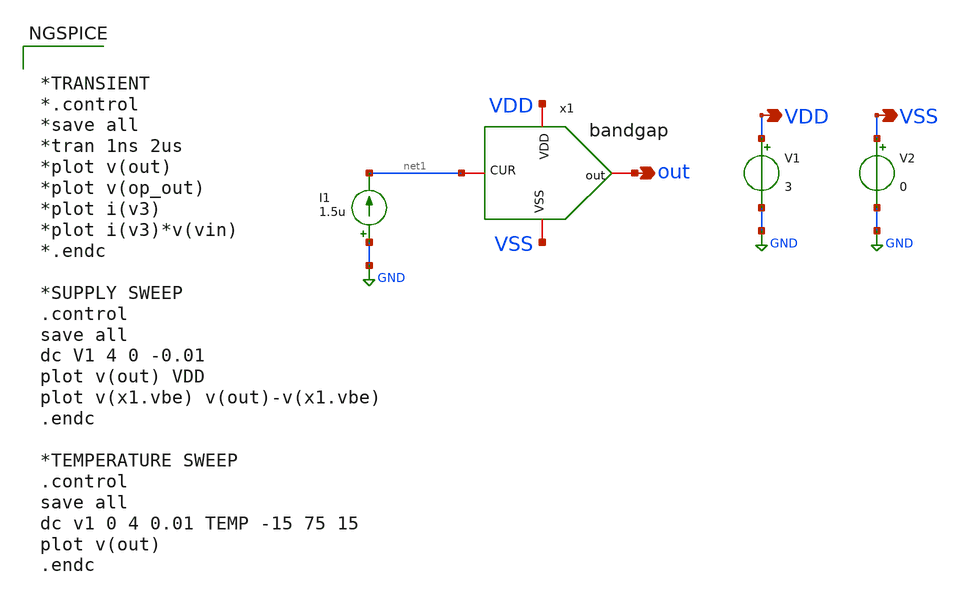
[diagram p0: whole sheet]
** sch_path: LDO/xschem/bandgap/bandgap-test.sch

.include $env(PDK_ROOT)/$env(PDK)/libs.tech/ngspice/design.ngspice
.lib $env(PDK_ROOT)/$env(PDK)/libs.tech/ngspice/sm141064.ngspice typical
.lib $env(PDK_ROOT)/$env(PDK)/libs.tech/ngspice/sm141064.ngspice mimcap_statistical
.lib $env(PDK_ROOT)/$env(PDK)/libs.tech/ngspice/sm141064.ngspice cap_mim
.lib $env(PDK_ROOT)/$env(PDK)/libs.tech/ngspice/sm141064.ngspice res_typical
.lib $env(PDK_ROOT)/$env(PDK)/libs.tech/ngspice/sm141064.ngspice bjt_typical
.lib $env(PDK_ROOT)/$env(PDK)/libs.tech/ngspice/sm141064.ngspice moscap_typical

**.subckt bandgap-test VDD VSS out
*.opin VDD
*.opin VSS
*.opin out
V1 VDD GND 3
V2 VSS GND 0
I1 GND net1 1.5u
x1 VDD out net1 VSS bandgap
**** begin user architecture code


*TRANSIENT
*.control
*save all
*tran 1ns 2us
*plot v(out)
*plot v(op_out)
*plot i(v3)
*plot i(v3)*v(vin)
*.endc

*SUPPLY SWEEP
.control
save all
dc V1 4 0 -0.01
plot v(out) VDD
plot v(x1.vbe) v(out)-v(x1.vbe)
.endc

*TEMPERATURE SWEEP
.control
save all
dc v1 0 4 0.01 TEMP -15 75 15
plot v(out)
.endc


**** end user architecture code
**.ends
.GLOBAL GND
.end
